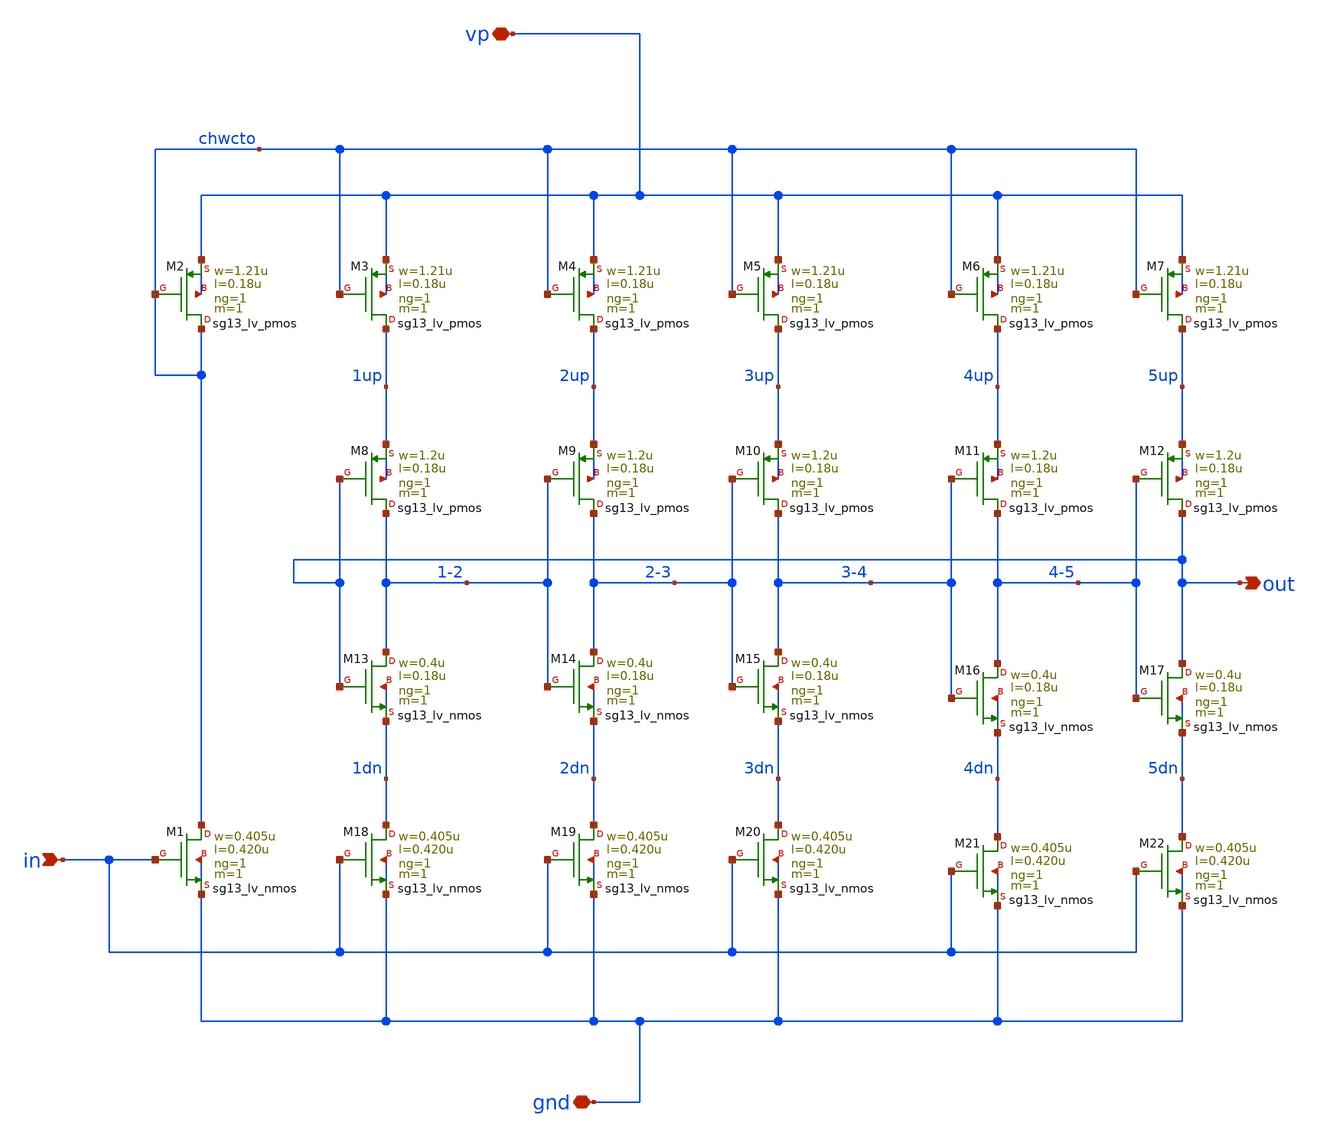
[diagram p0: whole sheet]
** sch_path: schematics/vco/vco_cell/vco_cell.sch
**.subckt vco_cell in gnd vp out
*.ipin in
*.iopin gnd
*.iopin vp
*.opin out
XM1 chwcto in gnd gnd sg13_lv_nmos w=0.405u l=0.420u ng=1 m=1 mm_ok=1
XM2 chwcto chwcto vp vp sg13_lv_pmos w=1.21u l=0.18u ng=1 m=1 mm_ok=1
XM3 1up chwcto vp vp sg13_lv_pmos w=1.21u l=0.18u ng=1 m=1 mm_ok=1
XM4 2up chwcto vp vp sg13_lv_pmos w=1.21u l=0.18u ng=1 m=1 mm_ok=1
XM5 3up chwcto vp vp sg13_lv_pmos w=1.21u l=0.18u ng=1 m=1 mm_ok=1
XM6 4up chwcto vp vp sg13_lv_pmos w=1.21u l=0.18u ng=1 m=1 mm_ok=1
XM7 5up chwcto vp vp sg13_lv_pmos w=1.21u l=0.18u ng=1 m=1 mm_ok=1
XM8 1-2 out 1up 1up sg13_lv_pmos w=1.2u l=0.18u ng=1 m=1 mm_ok=1
XM9 2-3 1-2 2up 2up sg13_lv_pmos w=1.2u l=0.18u ng=1 m=1 mm_ok=1
XM10 3-4 2-3 3up 3up sg13_lv_pmos w=1.2u l=0.18u ng=1 m=1 mm_ok=1
XM11 4-5 3-4 4up 4up sg13_lv_pmos w=1.2u l=0.18u ng=1 m=1 mm_ok=1
XM12 out 4-5 5up 5up sg13_lv_pmos w=1.2u l=0.18u ng=1 m=1 mm_ok=1
XM13 1-2 out 1dn 1dn sg13_lv_nmos w=0.4u l=0.18u ng=1 m=1 mm_ok=1
XM14 2-3 1-2 2dn 2dn sg13_lv_nmos w=0.4u l=0.18u ng=1 m=1 mm_ok=1
XM15 3-4 2-3 3dn 3dn sg13_lv_nmos w=0.4u l=0.18u ng=1 m=1 mm_ok=1
XM16 4-5 3-4 4dn 4dn sg13_lv_nmos w=0.4u l=0.18u ng=1 m=1 mm_ok=1
XM17 out 4-5 5dn 5dn sg13_lv_nmos w=0.4u l=0.18u ng=1 m=1 mm_ok=1
XM18 1dn in gnd gnd sg13_lv_nmos w=0.405u l=0.420u ng=1 m=1 mm_ok=1
XM19 2dn in gnd gnd sg13_lv_nmos w=0.405u l=0.420u ng=1 m=1 mm_ok=1
XM20 3dn in gnd gnd sg13_lv_nmos w=0.405u l=0.420u ng=1 m=1 mm_ok=1
XM21 4dn in gnd gnd sg13_lv_nmos w=0.405u l=0.420u ng=1 m=1 mm_ok=1
XM22 5dn in gnd gnd sg13_lv_nmos w=0.405u l=0.420u ng=1 m=1 mm_ok=1
**.ends
.end
